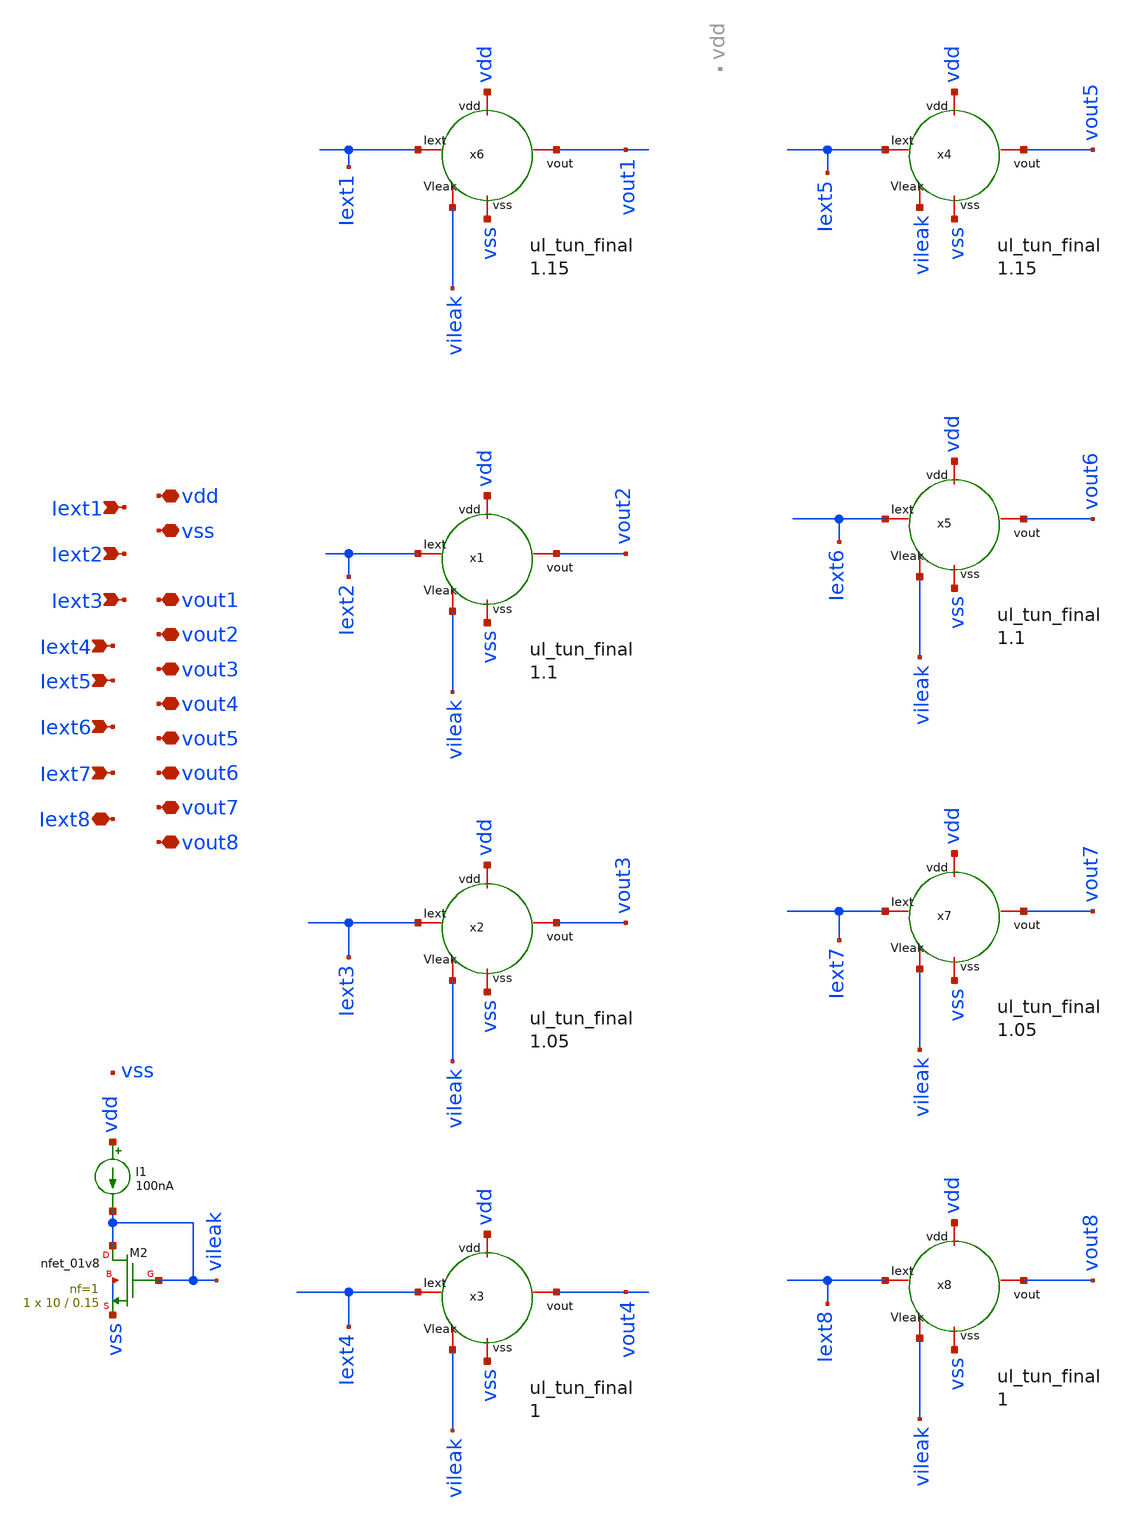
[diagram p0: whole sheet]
** sch_path: layer/layer_hidden.sch
**.subckt layer_hidden vdd vss Iext1 Iext2 Iext3 Iext4 vout1 vout2 vout3 vout4 Iext5 Iext6 Iext7
*+ Iext8 vout5 vout6 vout7 vout8
*.iopin vdd
*.iopin vss
*.ipin Iext1
*.ipin Iext2
*.ipin Iext3
*.ipin Iext4
*.iopin vout1
*.iopin vout2
*.iopin vout3
*.iopin vout4
*.ipin Iext5
*.ipin Iext6
*.ipin Iext7
*.iopin Iext8
*.iopin vout5
*.iopin vout6
*.iopin vout7
*.iopin vout8
Xx6 Iext1 vdd vout1 vileak vss ul_tun_final W_LEAK=1.15 CM=0.8p
XM2 vileak vileak vss vss sky130_fd_pr__nfet_01v8 L=0.15 W=10 nf=1 ad='int((nf+1)/2) * W/nf * 0.29' as='int((nf+2)/2) * W/nf * 0.29'
+ pd='2*int((nf+1)/2) * (W/nf + 0.29)' ps='2*int((nf+2)/2) * (W/nf + 0.29)' nrd='0.29 / W' nrs='0.29 / W'
+ sa=0 sb=0 sd=0 mult=1 m=1
I1 vdd vileak 100nA
Xx1 Iext2 vdd vout2 vileak vss ul_tun_final W_LEAK=1.1 CM=0.8p
Xx2 Iext3 vdd vout3 vileak vss ul_tun_final W_LEAK=1.05 CM=0.8p
Xx3 Iext4 vdd vout4 vileak vss ul_tun_final W_LEAK=1 CM=0.8p
Xx8 Iext8 vdd vout8 vileak vss ul_tun_final W_LEAK=1 CM=0.8p
Xx4 Iext5 vdd vout5 vileak vss ul_tun_final W_LEAK=1.15 CM=0.8p
Xx5 Iext6 vdd vout6 vileak vss ul_tun_final W_LEAK=1.1 CM=0.8p
Xx7 Iext7 vdd vout7 vileak vss ul_tun_final W_LEAK=1.05 CM=0.8p
**.ends
.end
